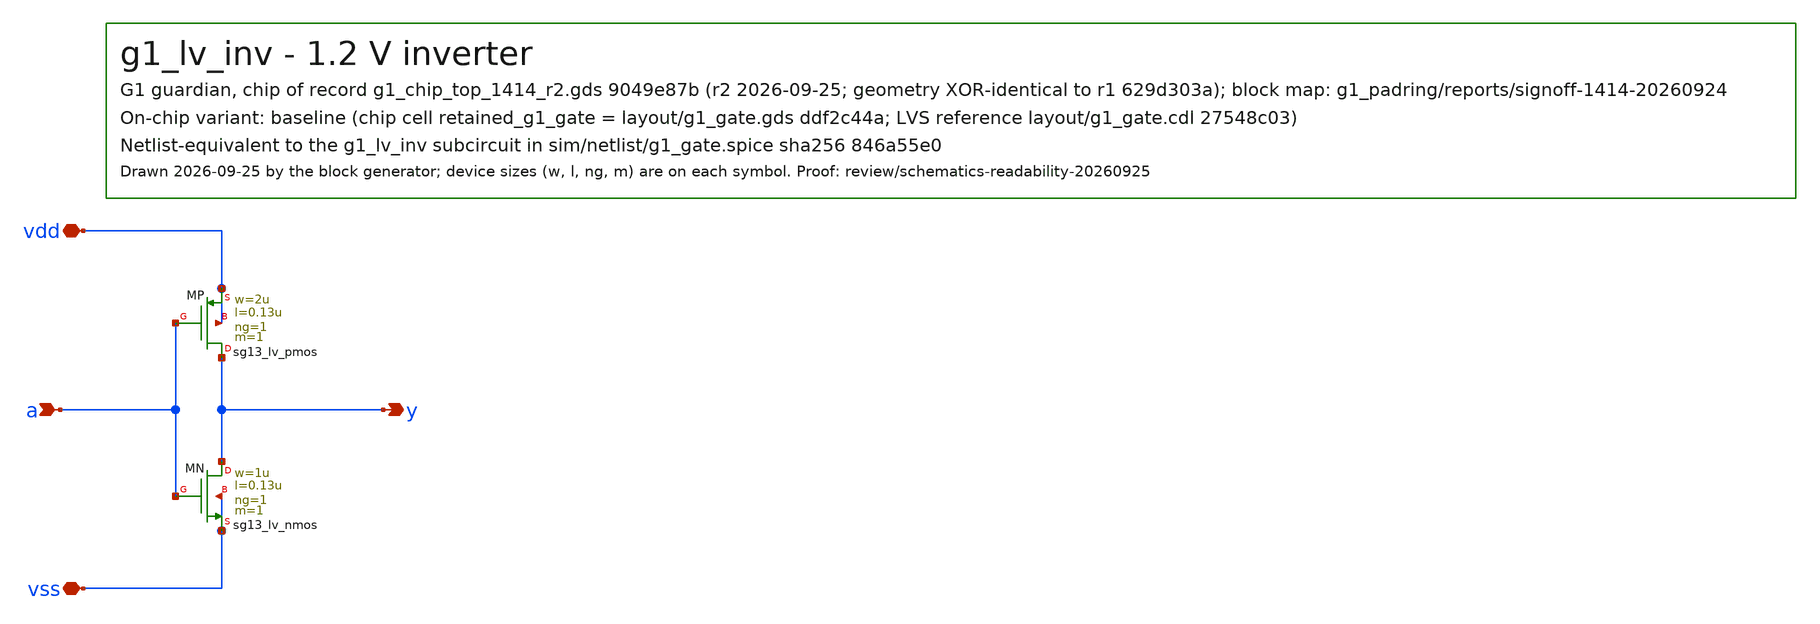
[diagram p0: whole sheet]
** sch_path: designs/g1-guardian/blocks/g1_gate/schematic/g1_lv_inv.sch
**.subckt g1_lv_inv a y vdd vss
*.ipin a
*.opin y
*.iopin vdd
*.iopin vss
XMP y a vdd vdd sg13_lv_pmos w=2u l=0.13u ng=1 m=1 mm_ok=1
XMN y a vss vss sg13_lv_nmos w=1u l=0.13u ng=1 m=1 mm_ok=1
**.ends
.end
